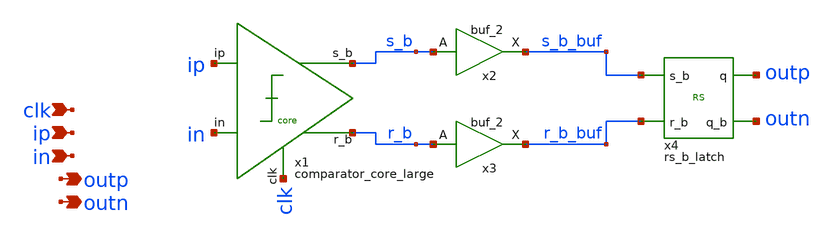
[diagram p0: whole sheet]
** sch_path: design/analog_modulator/schematic/comparator.sch
**.subckt comparator clk ip in outp outn
*.ipin clk
*.ipin ip
*.ipin in
*.opin outp
*.opin outn
x2 s_b VSS VSS VDD VDD s_b_buf sky130_fd_sc_hd__buf_2
x3 r_b VSS VSS VDD VDD r_b_buf sky130_fd_sc_hd__buf_2
x4 s_b_buf r_b_buf outp outn VDD VSS rs_b_latch
x1 ip in s_b clk r_b VDD VSS comparator_core_large
**.ends
.end
